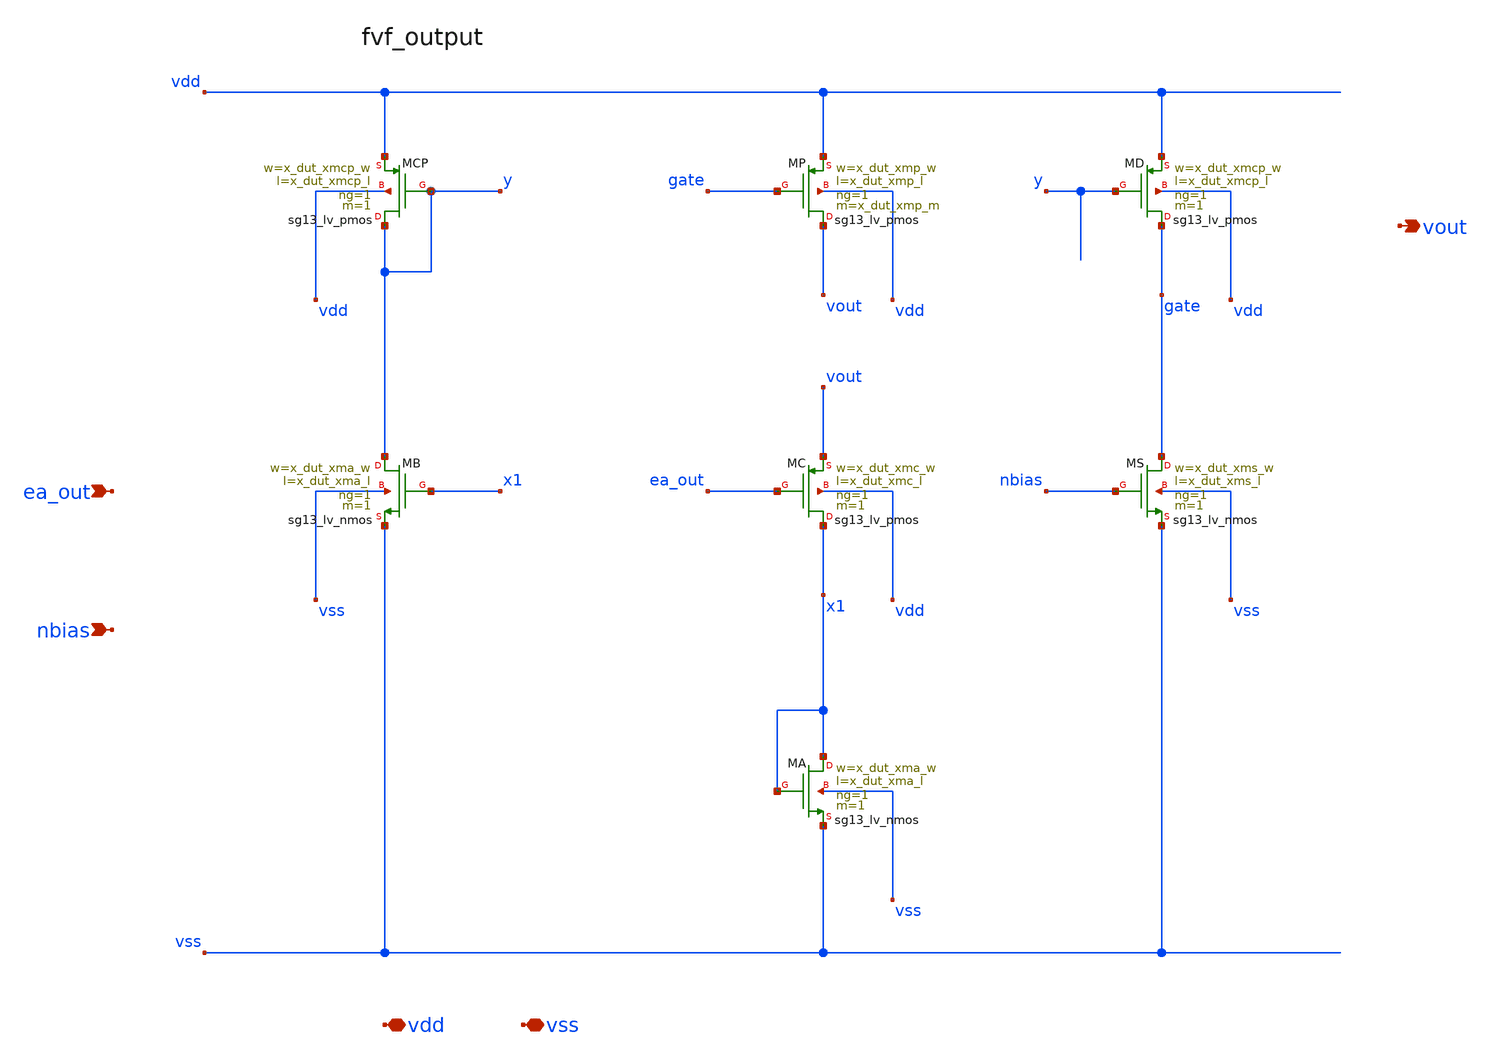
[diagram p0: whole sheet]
** sch_path: circuits/ldo_ihp_capless/xschem/blocks/fvf_output.sch
**.subckt fvf_output ea_out nbias vdd vss vout
*.ipin ea_out
*.ipin nbias
*.iopin vdd
*.iopin vss
*.opin vout
XMC x1 ea_out vout vdd sg13_lv_pmos w=x_dut_xmc_w l=x_dut_xmc_l ng=1 m=1 mm_ok=1
XMA x1 x1 vss vss sg13_lv_nmos w=x_dut_xma_w l=x_dut_xma_l ng=1 m=1 mm_ok=1
XMB y x1 vss vss sg13_lv_nmos w=x_dut_xma_w l=x_dut_xma_l ng=1 m=1 mm_ok=1
XMCP y y vdd vdd sg13_lv_pmos w=x_dut_xmcp_w l=x_dut_xmcp_l ng=1 m=1 mm_ok=1
XMD gate y vdd vdd sg13_lv_pmos w=x_dut_xmcp_w l=x_dut_xmcp_l ng=1 m=1 mm_ok=1
XMS gate nbias vss vss sg13_lv_nmos w=x_dut_xms_w l=x_dut_xms_l ng=1 m=1 mm_ok=1
XMP vout gate vdd vdd sg13_lv_pmos w=x_dut_xmp_w l=x_dut_xmp_l ng=1 m=x_dut_xmp_m mm_ok=1
**.ends
.end
